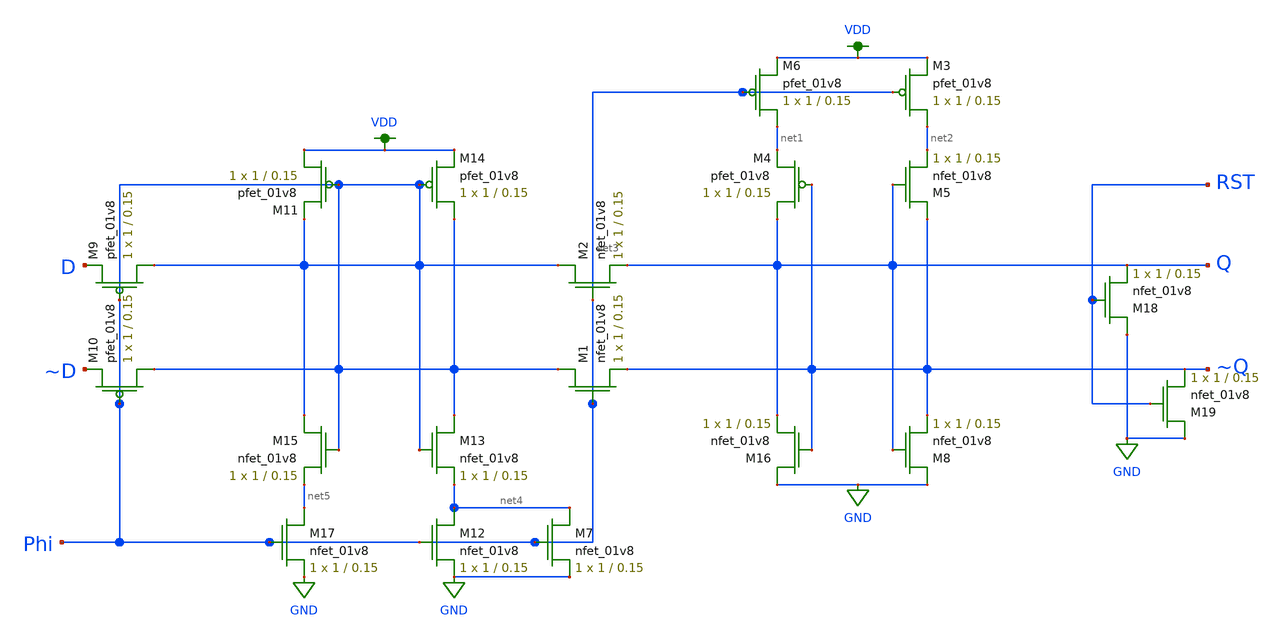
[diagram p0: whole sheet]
** sch_path: shift register/full_shift_register.sch
**.subckt full_shift_register
XM17 net5 Phi GND GND sky130_fd_pr__nfet_01v8 L=0.15 W=1 nf=1 ad='int((nf+1)/2) * W/nf * 0.29' as='int((nf+2)/2) * W/nf * 0.29'
+ pd='2*int((nf+1)/2) * (W/nf + 0.29)' ps='2*int((nf+2)/2) * (W/nf + 0.29)' nrd='0.29 / W' nrs='0.29 / W'
+ sa=0 sb=0 sd=0 mult=1 m=1
XM12 net4 Phi GND GND sky130_fd_pr__nfet_01v8 L=0.15 W=1 nf=1 ad='int((nf+1)/2) * W/nf * 0.29' as='int((nf+2)/2) * W/nf * 0.29'
+ pd='2*int((nf+1)/2) * (W/nf + 0.29)' ps='2*int((nf+2)/2) * (W/nf + 0.29)' nrd='0.29 / W' nrs='0.29 / W'
+ sa=0 sb=0 sd=0 mult=1 m=1
XM13 Phi Phi net4 GND sky130_fd_pr__nfet_01v8 L=0.15 W=1 nf=1 ad='int((nf+1)/2) * W/nf * 0.29' as='int((nf+2)/2) * W/nf * 0.29'
+ pd='2*int((nf+1)/2) * (W/nf + 0.29)' ps='2*int((nf+2)/2) * (W/nf + 0.29)' nrd='0.29 / W' nrs='0.29 / W'
+ sa=0 sb=0 sd=0 mult=1 m=1
XM15 Phi Phi net5 GND sky130_fd_pr__nfet_01v8 L=0.15 W=1 nf=1 ad='int((nf+1)/2) * W/nf * 0.29' as='int((nf+2)/2) * W/nf * 0.29'
+ pd='2*int((nf+1)/2) * (W/nf + 0.29)' ps='2*int((nf+2)/2) * (W/nf + 0.29)' nrd='0.29 / W' nrs='0.29 / W'
+ sa=0 sb=0 sd=0 mult=1 m=1
XM1 Phi net3 ~Q GND sky130_fd_pr__nfet_01v8 L=0.15 W=1 nf=1 ad='int((nf+1)/2) * W/nf * 0.29' as='int((nf+2)/2) * W/nf * 0.29'
+ pd='2*int((nf+1)/2) * (W/nf + 0.29)' ps='2*int((nf+2)/2) * (W/nf + 0.29)' nrd='0.29 / W' nrs='0.29 / W'
+ sa=0 sb=0 sd=0 mult=1 m=1
XM2 Phi net3 Q GND sky130_fd_pr__nfet_01v8 L=0.15 W=1 nf=1 ad='int((nf+1)/2) * W/nf * 0.29' as='int((nf+2)/2) * W/nf * 0.29'
+ pd='2*int((nf+1)/2) * (W/nf + 0.29)' ps='2*int((nf+2)/2) * (W/nf + 0.29)' nrd='0.29 / W' nrs='0.29 / W'
+ sa=0 sb=0 sd=0 mult=1 m=1
XM8 GND Q ~Q GND sky130_fd_pr__nfet_01v8 L=0.15 W=1 nf=1 ad='int((nf+1)/2) * W/nf * 0.29' as='int((nf+2)/2) * W/nf * 0.29'
+ pd='2*int((nf+1)/2) * (W/nf + 0.29)' ps='2*int((nf+2)/2) * (W/nf + 0.29)' nrd='0.29 / W' nrs='0.29 / W'
+ sa=0 sb=0 sd=0 mult=1 m=1
XM4 Q ~Q net1 VDD sky130_fd_pr__pfet_01v8 L=0.15 W=1 nf=1 ad='int((nf+1)/2) * W/nf * 0.29' as='int((nf+2)/2) * W/nf * 0.29'
+ pd='2*int((nf+1)/2) * (W/nf + 0.29)' ps='2*int((nf+2)/2) * (W/nf + 0.29)' nrd='0.29 / W' nrs='0.29 / W'
+ sa=0 sb=0 sd=0 mult=1 m=1
XM3 net2 net3 VDD VDD sky130_fd_pr__pfet_01v8 L=0.15 W=1 nf=1 ad='int((nf+1)/2) * W/nf * 0.29' as='int((nf+2)/2) * W/nf * 0.29'
+ pd='2*int((nf+1)/2) * (W/nf + 0.29)' ps='2*int((nf+2)/2) * (W/nf + 0.29)' nrd='0.29 / W' nrs='0.29 / W'
+ sa=0 sb=0 sd=0 mult=1 m=1
XM6 net1 net3 VDD VDD sky130_fd_pr__pfet_01v8 L=0.15 W=1 nf=1 ad='int((nf+1)/2) * W/nf * 0.29' as='int((nf+2)/2) * W/nf * 0.29'
+ pd='2*int((nf+1)/2) * (W/nf + 0.29)' ps='2*int((nf+2)/2) * (W/nf + 0.29)' nrd='0.29 / W' nrs='0.29 / W'
+ sa=0 sb=0 sd=0 mult=1 m=1
XM10 Phi Phi ~D VDD sky130_fd_pr__pfet_01v8 L=0.15 W=1 nf=1 ad='int((nf+1)/2) * W/nf * 0.29' as='int((nf+2)/2) * W/nf * 0.29'
+ pd='2*int((nf+1)/2) * (W/nf + 0.29)' ps='2*int((nf+2)/2) * (W/nf + 0.29)' nrd='0.29 / W' nrs='0.29 / W'
+ sa=0 sb=0 sd=0 mult=1 m=1
XM9 Phi Phi D VDD sky130_fd_pr__pfet_01v8 L=0.15 W=1 nf=1 ad='int((nf+1)/2) * W/nf * 0.29' as='int((nf+2)/2) * W/nf * 0.29'
+ pd='2*int((nf+1)/2) * (W/nf + 0.29)' ps='2*int((nf+2)/2) * (W/nf + 0.29)' nrd='0.29 / W' nrs='0.29 / W'
+ sa=0 sb=0 sd=0 mult=1 m=1
XM11 VDD Phi Phi VDD sky130_fd_pr__pfet_01v8 L=0.15 W=1 nf=1 ad='int((nf+1)/2) * W/nf * 0.29' as='int((nf+2)/2) * W/nf * 0.29'
+ pd='2*int((nf+1)/2) * (W/nf + 0.29)' ps='2*int((nf+2)/2) * (W/nf + 0.29)' nrd='0.29 / W' nrs='0.29 / W'
+ sa=0 sb=0 sd=0 mult=1 m=1
XM14 Phi Phi VDD VDD sky130_fd_pr__pfet_01v8 L=0.15 W=1 nf=1 ad='int((nf+1)/2) * W/nf * 0.29' as='int((nf+2)/2) * W/nf * 0.29'
+ pd='2*int((nf+1)/2) * (W/nf + 0.29)' ps='2*int((nf+2)/2) * (W/nf + 0.29)' nrd='0.29 / W' nrs='0.29 / W'
+ sa=0 sb=0 sd=0 mult=1 m=1
XM16 GND ~Q Q GND sky130_fd_pr__nfet_01v8 L=0.15 W=1 nf=1 ad='int((nf+1)/2) * W/nf * 0.29' as='int((nf+2)/2) * W/nf * 0.29'
+ pd='2*int((nf+1)/2) * (W/nf + 0.29)' ps='2*int((nf+2)/2) * (W/nf + 0.29)' nrd='0.29 / W' nrs='0.29 / W'
+ sa=0 sb=0 sd=0 mult=1 m=1
XM5 ~Q Q net2 GND sky130_fd_pr__nfet_01v8 L=0.15 W=1 nf=1 ad='int((nf+1)/2) * W/nf * 0.29' as='int((nf+2)/2) * W/nf * 0.29'
+ pd='2*int((nf+1)/2) * (W/nf + 0.29)' ps='2*int((nf+2)/2) * (W/nf + 0.29)' nrd='0.29 / W' nrs='0.29 / W'
+ sa=0 sb=0 sd=0 mult=1 m=1
XM7 net4 net3 GND GND sky130_fd_pr__nfet_01v8 L=0.15 W=1 nf=1 ad='int((nf+1)/2) * W/nf * 0.29' as='int((nf+2)/2) * W/nf * 0.29'
+ pd='2*int((nf+1)/2) * (W/nf + 0.29)' ps='2*int((nf+2)/2) * (W/nf + 0.29)' nrd='0.29 / W' nrs='0.29 / W'
+ sa=0 sb=0 sd=0 mult=1 m=1
XM18 GND RST Q GND sky130_fd_pr__nfet_01v8 L=0.15 W=1 nf=1 ad='int((nf+1)/2) * W/nf * 0.29' as='int((nf+2)/2) * W/nf * 0.29'
+ pd='2*int((nf+1)/2) * (W/nf + 0.29)' ps='2*int((nf+2)/2) * (W/nf + 0.29)' nrd='0.29 / W' nrs='0.29 / W'
+ sa=0 sb=0 sd=0 mult=1 m=1
XM19 GND RST ~Q GND sky130_fd_pr__nfet_01v8 L=0.15 W=1 nf=1 ad='int((nf+1)/2) * W/nf * 0.29' as='int((nf+2)/2) * W/nf * 0.29'
+ pd='2*int((nf+1)/2) * (W/nf + 0.29)' ps='2*int((nf+2)/2) * (W/nf + 0.29)' nrd='0.29 / W' nrs='0.29 / W'
+ sa=0 sb=0 sd=0 mult=1 m=1
**.ends
.GLOBAL GND
.GLOBAL VDD
.end
